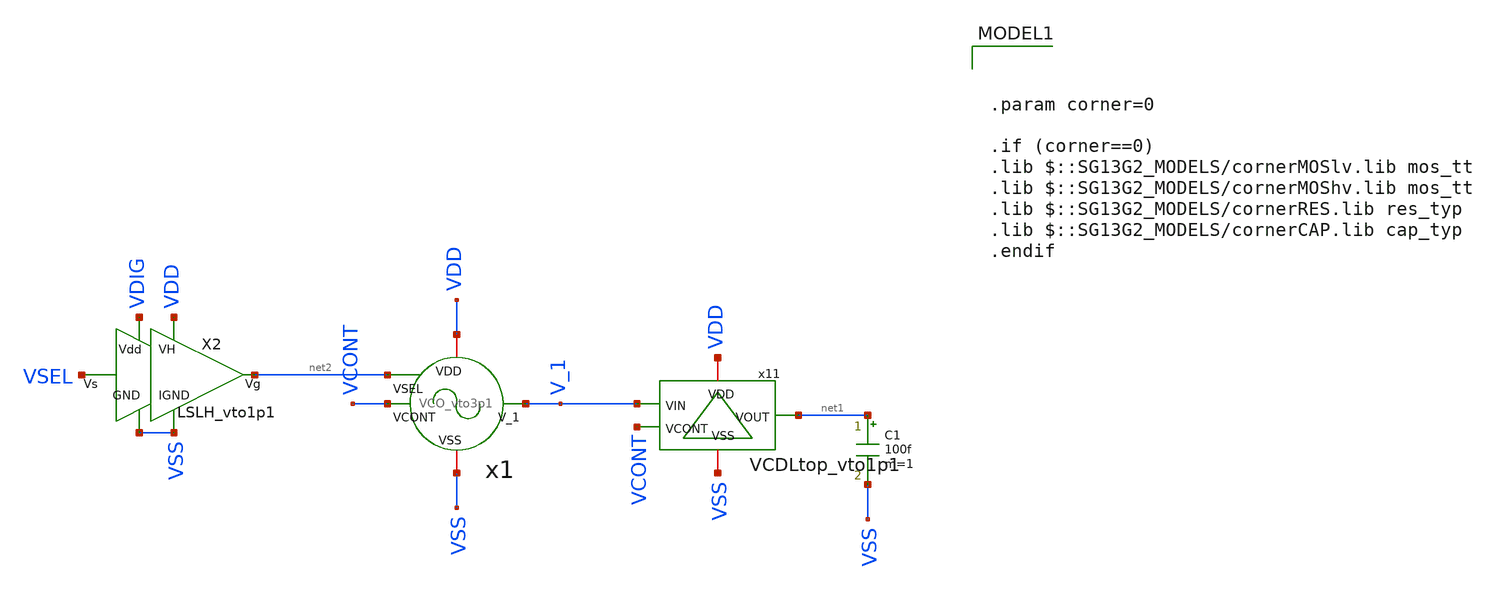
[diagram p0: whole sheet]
** sch_path: ChipUSM_AnalogTrack24/VCO/tb_VCO_vto3p1.sch
**.subckt tb_VCO_vto3p1
x1 VCONT VSS VDD V_1 net2 VCO_vto3p1
x11 V_1 VCONT net1 VSS VDD VCDLtop_vto1p1
C1 net1 VSS 100f m=1
X2 VSEL net2 VDIG VDD VSS VSS LSLH_vto1p1
**** begin user architecture code


vvsel vsel 0 dc 1.2
vvdd vdd 0 dc 3.3
vvdig vdig 0 dc 1.2
vvss vss 0 0
vvcont VCONT 0 dc 0.6
*.option temp = 200
.ic v(V_1) = 0
.ic v(x1.V_2) = 3.3
.save v(V_1)
*.save v(V_1) v(x1.v_1_int) v(v_2) v(x1.v_3) v(x1.v_4) v(x1.v_5)

.option method=gear
*.option cshunt=0.05e-12

.OPTION ABSTOL=1e-15.
.OPTION GMIN=1.0e-12.
.OPTION ITL1=1e5
.OPTION RSHUNT=1e12
.OPTION RELTOL=1e-5

.control
   compose vin_var start=0.1 stop=2.2 step=0.2
   foreach val $&vin_var
     alter vvcont $val
     tran 5n 10u
   end
wrdata
+ /home/designer/shared/TORepo_IHPNov2024_TDBuck/design_data/xschem/sim_data/data_VCO_vto3p1.txt tran1.v(V_1) tran2.v(V_1) tran3.v(V_1) tran4.v(V_1) tran5.v(V_1) tran6.v(V_1) tran7.v(V_1)
+ tran8.v(V_1) tran9.v(V_1) tran10.v(V_1) tran11.v(V_1)
plot tran1.v(V_1) (tran6.v(V_1)+4) (tran11.v(V_1)+8)

*tran 5n 5u
*plot v(x1.v_1_int) v(v_2) v(x1.v_3) v(x1.v_4) v(x1.v_5)

.endc

*.measure tran tdelay
*+ TRIG v(x1.v_1_int) TD=4u VAL=1.65 RISE=1
*+ TARG v(x1.v_1_int) TD=4u VAL=1.65 RISE=2
*.measure tran tdelay_buff
*+ TRIG v(x1.v_1_int) TD=4u VAL=1.65 RISE=1
*+ TARG v(v_1) TD=4u VAL=1.65 RISE=1





.param corner=0

.if (corner==0)
.lib $::SG13G2_MODELS/cornerMOSlv.lib mos_tt
.lib $::SG13G2_MODELS/cornerMOShv.lib mos_tt
.lib $::SG13G2_MODELS/cornerRES.lib res_typ
.lib $::SG13G2_MODELS/cornerCAP.lib cap_typ
.endif

**** end user architecture code
**.ends
.end
